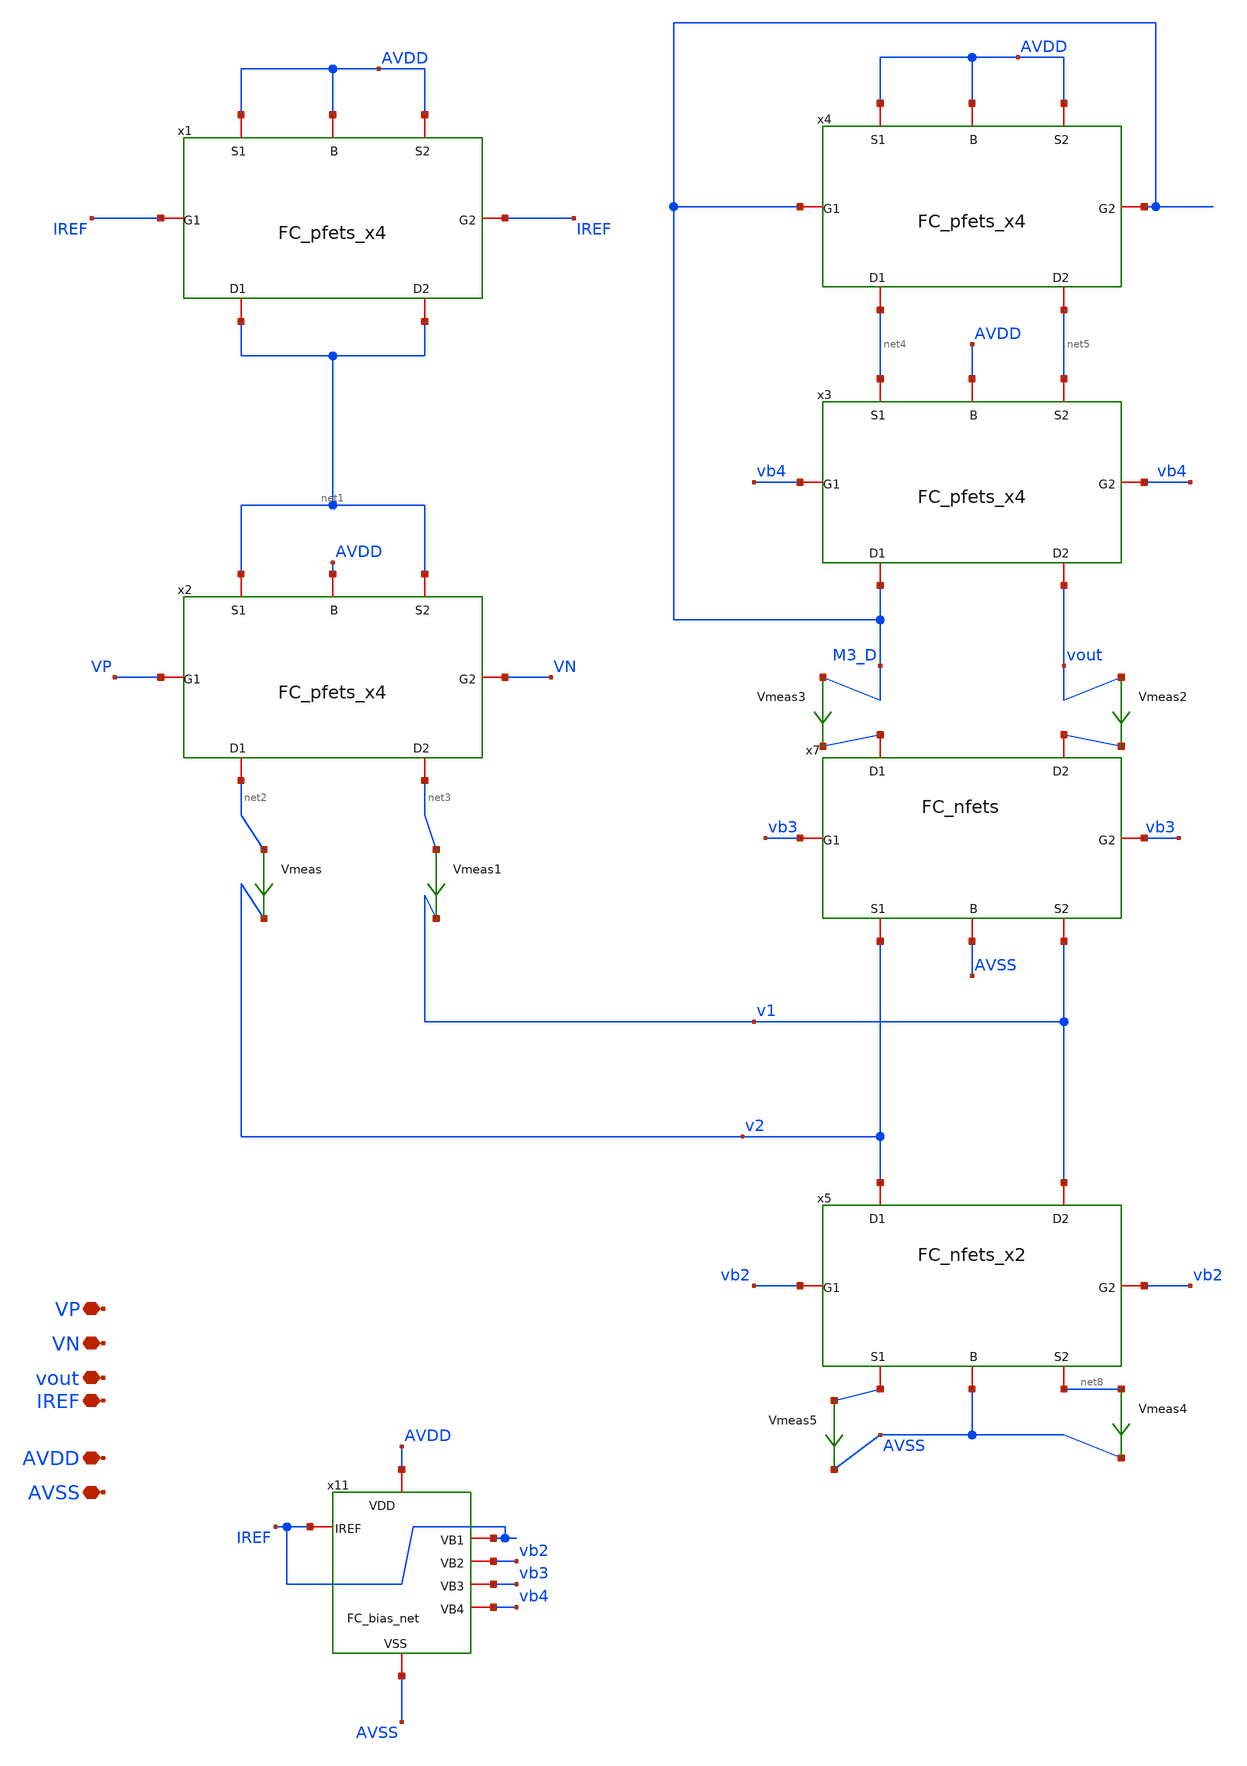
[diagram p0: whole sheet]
** sch_path: TIA_Filter/Folded/FoldedCascode.sch
**.subckt FoldedCascode AVDD AVSS vout VP VN IREF
*.iopin AVDD
*.iopin AVSS
*.iopin vout
*.iopin VP
*.iopin VN
*.iopin IREF
x7 v2 v1 net6 net7 vb3 vb3 AVSS FC_nfets
x5 net9 net8 v2 v1 vb2 vb2 AVSS FC_nfets_x2
x1 AVDD AVDD net1 net1 IREF IREF AVDD FC_pfets_x4
x2 net1 net1 net2 net3 VP VN AVDD FC_pfets_x4
x3 net4 net5 M3_D vout vb4 vb4 AVDD FC_pfets_x4
x4 AVDD AVDD net4 net5 M3_D M3_D AVDD FC_pfets_x4
x11 IREF IREF vb2 vb3 vb4 AVDD AVSS FC_bias_net
Vmeas net2 v2 0
.save i(vmeas)
Vmeas1 net3 v1 0
.save i(vmeas1)
Vmeas2 vout net7 0
.save i(vmeas2)
Vmeas3 M3_D net6 0
.save i(vmeas3)
Vmeas4 net8 AVSS 0
.save i(vmeas4)
Vmeas5 net9 AVSS 0
.save i(vmeas5)
**.ends
.end
